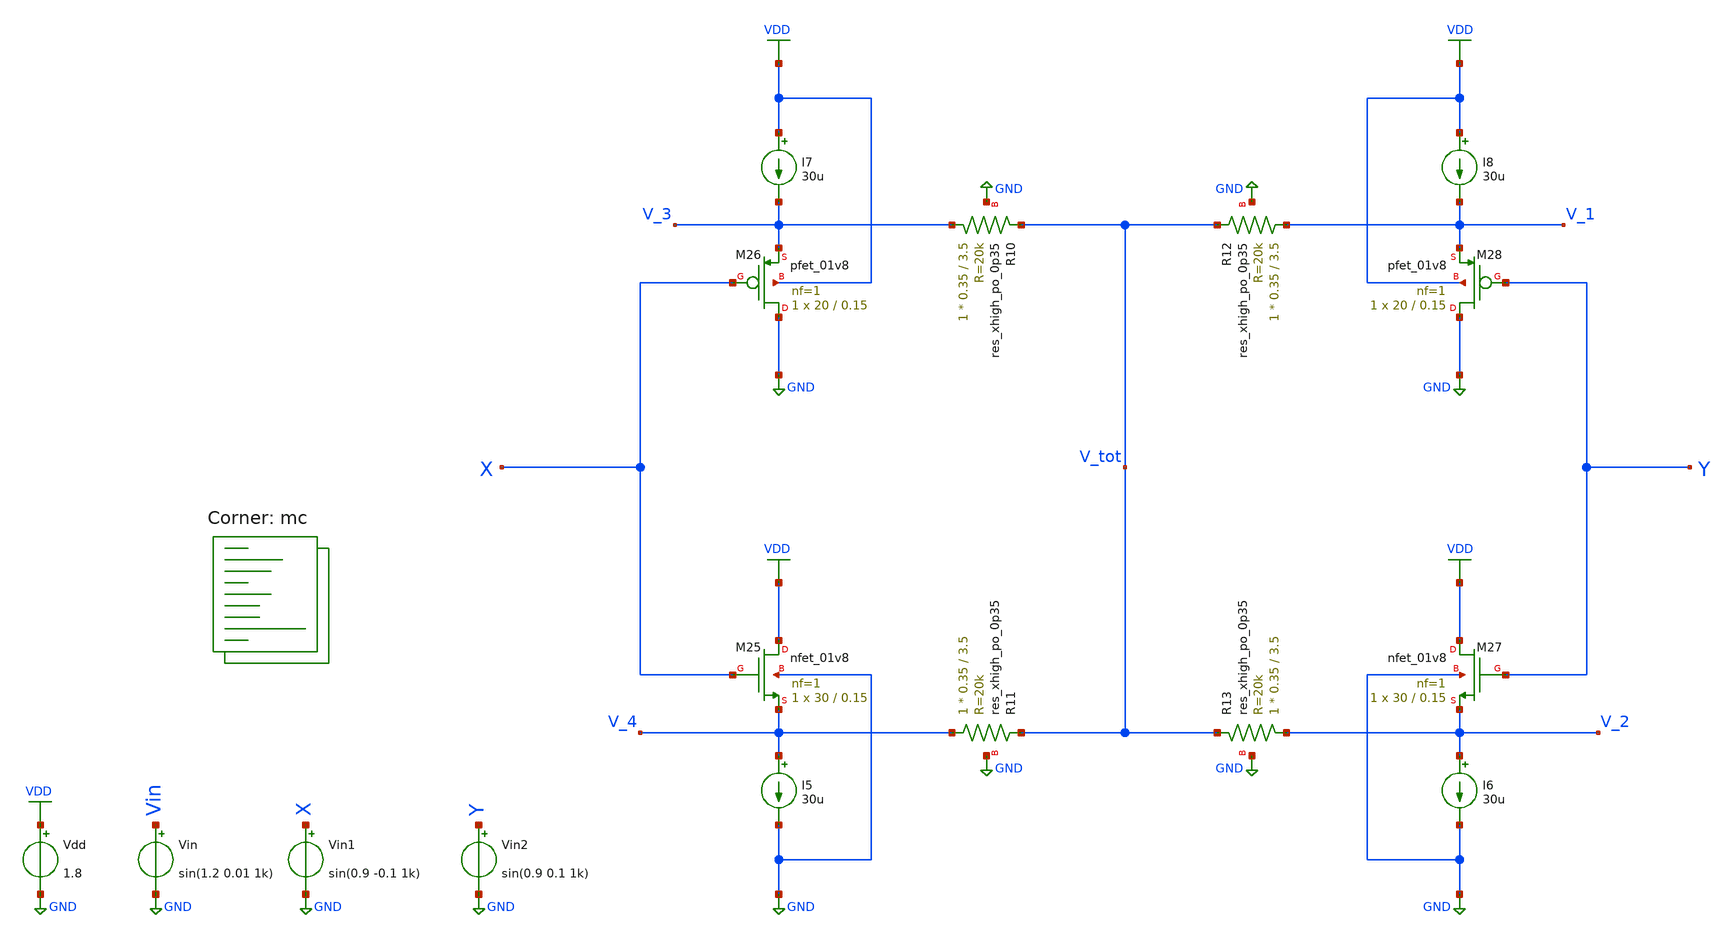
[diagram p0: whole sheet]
** sch_path: projects/montecarlo/xschem_ngspice/inverter/common_drain_mc.sch
**.subckt common_drain_mc
Vdd VDD GND 1.8
Vin Vin GND sin(1.2 0.01 1k)
XM25 VDD X V_4 GND sky130_fd_pr__nfet_01v8 L=0.15 W=30 nf=1 ad='int((nf+1)/2) * W/nf * 0.29' as='int((nf+2)/2) * W/nf * 0.29'
+ pd='2*int((nf+1)/2) * (W/nf + 0.29)' ps='2*int((nf+2)/2) * (W/nf + 0.29)' nrd='0.29 / W' nrs='0.29 / W'
+ sa=0 sb=0 sd=0 mult=1 m=1
XM26 GND X V_3 VDD sky130_fd_pr__pfet_01v8 L=0.15 W=20 nf=1 ad='int((nf+1)/2) * W/nf * 0.29' as='int((nf+2)/2) * W/nf * 0.29'
+ pd='2*int((nf+1)/2) * (W/nf + 0.29)' ps='2*int((nf+2)/2) * (W/nf + 0.29)' nrd='0.29 / W' nrs='0.29 / W'
+ sa=0 sb=0 sd=0 mult=1 m=1
XR10 V_3 V_tot GND sky130_fd_pr__res_xhigh_po_0p35 L=3.5 mult=1 m=1
XR11 V_4 V_tot GND sky130_fd_pr__res_xhigh_po_0p35 L=3.5 mult=1 m=1
XR12 V_1 V_tot GND sky130_fd_pr__res_xhigh_po_0p35 L=3.5 mult=1 m=1
XR13 V_2 V_tot GND sky130_fd_pr__res_xhigh_po_0p35 L=3.5 mult=1 m=1
XM27 VDD Y V_2 GND sky130_fd_pr__nfet_01v8 L=0.15 W=30 nf=1 ad='int((nf+1)/2) * W/nf * 0.29' as='int((nf+2)/2) * W/nf * 0.29'
+ pd='2*int((nf+1)/2) * (W/nf + 0.29)' ps='2*int((nf+2)/2) * (W/nf + 0.29)' nrd='0.29 / W' nrs='0.29 / W'
+ sa=0 sb=0 sd=0 mult=1 m=1
XM28 GND Y V_1 VDD sky130_fd_pr__pfet_01v8 L=0.15 W=20 nf=1 ad='int((nf+1)/2) * W/nf * 0.29' as='int((nf+2)/2) * W/nf * 0.29'
+ pd='2*int((nf+1)/2) * (W/nf + 0.29)' ps='2*int((nf+2)/2) * (W/nf + 0.29)' nrd='0.29 / W' nrs='0.29 / W'
+ sa=0 sb=0 sd=0 mult=1 m=1
I5 V_4 GND 30u
I6 V_2 GND 30u
I7 VDD V_3 30u
I8 VDD V_1 30u
Vin1 X GND sin(0.9 -0.1 1k)
Vin2 Y GND sin(0.9 0.1 1k)
**** begin user architecture code



.option wnflag=1
.option savecurrents
.save @m.xm1.msky130_fd_pr__nfet_01v8[gm] @m.xm1.msky130_fd_pr__nfet_01v8[vth] @m.xm2.msky130_fd_pr__pfet_01v8[gm] @m.xm2.msky130_fd_pr__pfet_01v8[vth]

.control

  let runs=20
  let run=1

  dowhile run <= runs
    save all
    * dc vin 0 1.8 0.01
    tran 1u 3m
    write common_source_mc.raw
    set appendwrite
    reset
    let run = run + 1
  end

.endc



.lib $::SKYWATER_MODELS/sky130.lib.spice mc
**** end user architecture code
**.ends
.GLOBAL GND
.GLOBAL VDD
.end
